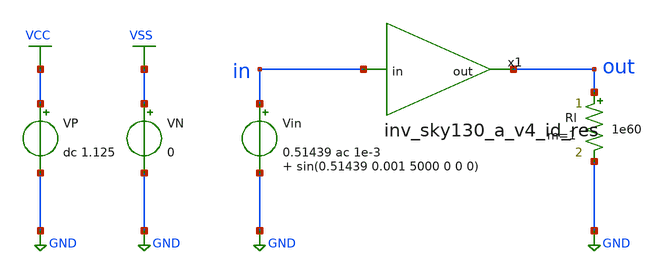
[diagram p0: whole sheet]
** sch_path: Amplifier_Inv/xschem/v4/tb_inv_sky130_a_sf_v4_id_res.sch
* StefanSchippers/xschem_sky130/sky130_tests/not.sch:
* Copyright 2021 Stefan Frederik Schippers
* Licensed under the Apache License, Version 2.0 (the "License");
**.subckt tb_inv_sky130_a_sf_v4_id_res
VN VSS GND 0
VP VCC GND dc 1.125
.save i(vp)
Vin in GND 0.51439 ac 1e-3 sin(0.51439 0.001 5000 0 0 0)
.save i(vin)
Rl out GND 1e60 m=1
x1 out in inv_sky130_a_v4_id_res
**** begin user architecture code

** opencircuitdesign pdks install
.lib $::SKYWATER_MODELS/sky130.lib.spice sf



.control

  op
  save all
  let gmn = @m.x1.x1.xm1.msky130_fd_pr__nfet_01v8[gm]
  let gmp = @m.x1.x1.xm2.msky130_fd_pr__pfet_01v8[gm]
  let gdsn = @m.x1.x1.xm1.msky130_fd_pr__nfet_01v8[gds]
  let gdsp = @m.x1.x1.xm2.msky130_fd_pr__pfet_01v8[gds]
  let cgsn = @m.x1.x1.xm1.msky130_fd_pr__nfet_01v8[cgs]
  let cgsp = @m.x1.x1.xm2.msky130_fd_pr__pfet_01v8[cgs]
  let cgdn = @m.x1.x1.xm1.msky130_fd_pr__nfet_01v8[cgd]
  let cgdp = @m.x1.x1.xm2.msky130_fd_pr__pfet_01v8[cgd]
  write tb_inv_sky130_a_op_sf_v4_id_res.raw gmn gmp gdsn gdsp cgsn cgsp cgdn cgdp

  ac dec 1000 1 1e8
  save all
  let gain = db(v(out)/v(in))
  let gain_vs1 = db(v(x1.vs1)/v(in))
  let phase = phase(v(out)/v(in))
  write tb_inv_sky130_a_AC_sf_v4_id_res.raw gain gain_vs1

  noise v(out) Vin dec 1000 300 10k 10
  save all
  write tb_inv_sky130_a_noise_sf_v4_id_res.raw

  noise v(out) Vin dec 1000 300 10k
  save all
  setplot noise1
  write tb_inv_sky130_a_noise_spectrum_sf_v4_id_res.raw

  dc Vin 0 1.125 0.00001
  save all v(out) v(x1.vs1) v(x1.vd1)
  write tb_inv_sky130_a_DC_sf_v4_id_res.raw v(out) v(x1.vs1) v(x1.vd1)

  tran 0.1u 4m
  save all
  let pw_in = i(Vin)*v(in)
  let pw_vcc = i(Vp)*1.125
  let pw_vg1 = i(Vg1)*0.725
  let pw_vg2 = i(Vg2)*1.085
  let pw_total = pw_in+pw_vcc
  meas tran avg_pw_total AVG pw_total FROM=0 TO=2m
  meas tran avg_pw_in AVG pw_in FROM=0 TO=2m
  meas tran avg_pw_vcc AVG pw_vcc FROM=0 TO=2m
  write tb_inv_sky130_a_tran_sf_v4_id_res.raw v(in) v(out) v(x1.vd1) v(x1.vs1) v(vg1) v(vg2)
+ avg_pw_total

  exit 0
.endc


**** end user architecture code
**.ends

* expanding   symbol:  v4/inv_sky130_a_v4_id_res.sym # of pins=2
** sym_path: Amplifier_Inv/xschem/v4/inv_sky130_a_v4_id_res.sym
** sch_path: Amplifier_Inv/xschem/v4/inv_sky130_a_v4_id_res.sch
.subckt inv_sky130_a_v4_id_res out in
*.ipin in
*.opin out
x1 VS1 VD1 VCC VSS not W_N=250 L_N=1 W_P=200 L_P=0.25 m=1
XC1 in VD1 sky130_fd_pr__cap_mim_m3_1 W=26 L=26 MF=1 m=1
XM3 GND out GND GND sky130_fd_pr__nfet_01v8 L=10 W=100 nf=1 ad='int((nf+1)/2) * W/nf * 0.29' as='int((nf+2)/2) * W/nf * 0.29'
+ pd='2*int((nf+1)/2) * (W/nf + 0.29)' ps='2*int((nf+2)/2) * (W/nf + 0.29)' nrd='0.29 / W' nrs='0.29 / W'
+ sa=0 sb=0 sd=0 mult=1 m=1
R1 VS1 VD1 3e9 m=1
R2 out VS1 8e6 m=1
.ends


* expanding   symbol:  sky130_tests/not.sym # of pins=2
** sym_path: sky130_tests/not.sym
** sch_path: sky130_tests/not.sch
.subckt not y a VCCPIN VSSPIN     W_N=1 L_N=0.15 W_P=2 L_P=0.15
*.opin y
*.ipin a
XM1 DN a VSSPIN VSSPIN sky130_fd_pr__nfet_01v8 L=L_N W=W_N nf=1 ad='int((1 + 1)/2) * W_N / 1 * 0.29'
+ as='int((1 + 2)/2) * W_N / 1 * 0.29' pd='2*int((1 + 1)/2) * (W_N / 1 + 0.29)' ps='2*int((1 + 2)/2) * (W_N / 1 + 0.29)'
+ nrd='0.29 / W_N ' nrs='0.29 / W_N ' sa=0 sb=0 sd=0 mult=1 m=1
XM2 DP a VCCPIN VCCPIN sky130_fd_pr__pfet_01v8 L=L_P W=W_P nf=1 ad='int((nf+1)/2) * W/nf * 0.29' as='int((nf+2)/2) * W/nf * 0.29'
+ pd='2*int((nf+1)/2) * (W/nf + 0.29)' ps='2*int((nf+2)/2) * (W/nf + 0.29)' nrd='0.29 / W' nrs='0.29 / W'
+ sa=0 sb=0 sd=0 mult=1 m=1
Vmeas DP y 0
.save i(vmeas)
Vmeas1 y DN 0
.save i(vmeas1)
.save v(dp)
.save v(dn)
.ends

.GLOBAL GND
.GLOBAL VSS
.GLOBAL VCC
.end
